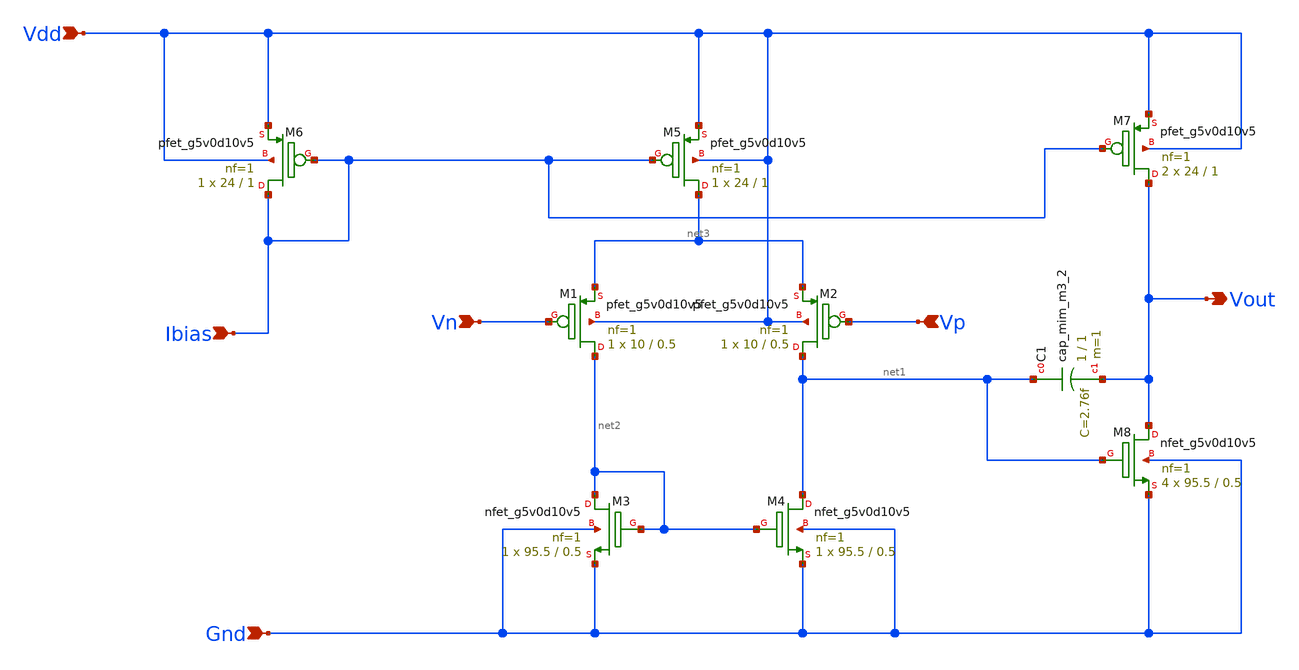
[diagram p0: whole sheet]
** sch_path: Analog_Blocks/OTA/Schematic/Miller_OTA_PMOS.sch
**.subckt Miller_OTA_PMOS Vout Ibias Vdd Gnd Vp Vn
*.opin Vout
*.ipin Ibias
*.ipin Vdd
*.ipin Gnd
*.ipin Vp
*.ipin Vn
XM6 Ibias Ibias Vdd Vdd sky130_fd_pr__pfet_g5v0d10v5 L=1 W=24 nf=1 ad='int((nf+1)/2) * W/nf * 0.29' as='int((nf+2)/2) * W/nf * 0.29'
+ pd='2*int((nf+1)/2) * (W/nf + 0.29)' ps='2*int((nf+2)/2) * (W/nf + 0.29)' nrd='0.29 / W' nrs='0.29 / W'
+ sa=0 sb=0 sd=0 mult=1 m=1
XM5 net3 Ibias Vdd Vdd sky130_fd_pr__pfet_g5v0d10v5 L=1 W=24 nf=1 ad='int((nf+1)/2) * W/nf * 0.29' as='int((nf+2)/2) * W/nf * 0.29'
+ pd='2*int((nf+1)/2) * (W/nf + 0.29)' ps='2*int((nf+2)/2) * (W/nf + 0.29)' nrd='0.29 / W' nrs='0.29 / W'
+ sa=0 sb=0 sd=0 mult=1 m=1
XM7 Vout Ibias Vdd Vdd sky130_fd_pr__pfet_g5v0d10v5 L=1 W=24 nf=1 ad='int((nf+1)/2) * W/nf * 0.29' as='int((nf+2)/2) * W/nf * 0.29'
+ pd='2*int((nf+1)/2) * (W/nf + 0.29)' ps='2*int((nf+2)/2) * (W/nf + 0.29)' nrd='0.29 / W' nrs='0.29 / W'
+ sa=0 sb=0 sd=0 mult=2 m=2
XM2 net1 Vp net3 Vdd sky130_fd_pr__pfet_g5v0d10v5 L=0.5 W=10 nf=1 ad='int((nf+1)/2) * W/nf * 0.29' as='int((nf+2)/2) * W/nf * 0.29'
+ pd='2*int((nf+1)/2) * (W/nf + 0.29)' ps='2*int((nf+2)/2) * (W/nf + 0.29)' nrd='0.29 / W' nrs='0.29 / W'
+ sa=0 sb=0 sd=0 mult=1 m=1
XM1 net2 Vn net3 Vdd sky130_fd_pr__pfet_g5v0d10v5 L=0.5 W=10 nf=1 ad='int((nf+1)/2) * W/nf * 0.29' as='int((nf+2)/2) * W/nf * 0.29'
+ pd='2*int((nf+1)/2) * (W/nf + 0.29)' ps='2*int((nf+2)/2) * (W/nf + 0.29)' nrd='0.29 / W' nrs='0.29 / W'
+ sa=0 sb=0 sd=0 mult=1 m=1
XM8 Vout net1 Gnd Gnd sky130_fd_pr__nfet_g5v0d10v5 L=0.5 W=95.5 nf=1 ad='int((nf+1)/2) * W/nf * 0.29'
+ as='int((nf+2)/2) * W/nf * 0.29' pd='2*int((nf+1)/2) * (W/nf + 0.29)' ps='2*int((nf+2)/2) * (W/nf + 0.29)'
+ nrd='0.29 / W' nrs='0.29 / W' sa=0 sb=0 sd=0 mult=4 m=4
XM4 net1 net2 Gnd Gnd sky130_fd_pr__nfet_g5v0d10v5 L=0.5 W=95.5 nf=1 ad='int((nf+1)/2) * W/nf * 0.29'
+ as='int((nf+2)/2) * W/nf * 0.29' pd='2*int((nf+1)/2) * (W/nf + 0.29)' ps='2*int((nf+2)/2) * (W/nf + 0.29)'
+ nrd='0.29 / W' nrs='0.29 / W' sa=0 sb=0 sd=0 mult=1 m=1
XM3 net2 net2 Gnd Gnd sky130_fd_pr__nfet_g5v0d10v5 L=0.5 W=95.5 nf=1 ad='int((nf+1)/2) * W/nf * 0.29'
+ as='int((nf+2)/2) * W/nf * 0.29' pd='2*int((nf+1)/2) * (W/nf + 0.29)' ps='2*int((nf+2)/2) * (W/nf + 0.29)'
+ nrd='0.29 / W' nrs='0.29 / W' sa=0 sb=0 sd=0 mult=1 m=1
XC1 net1 Vout sky130_fd_pr__cap_mim_m3_2 W=1 L=1 MF=1 m=1
**.ends
.end
